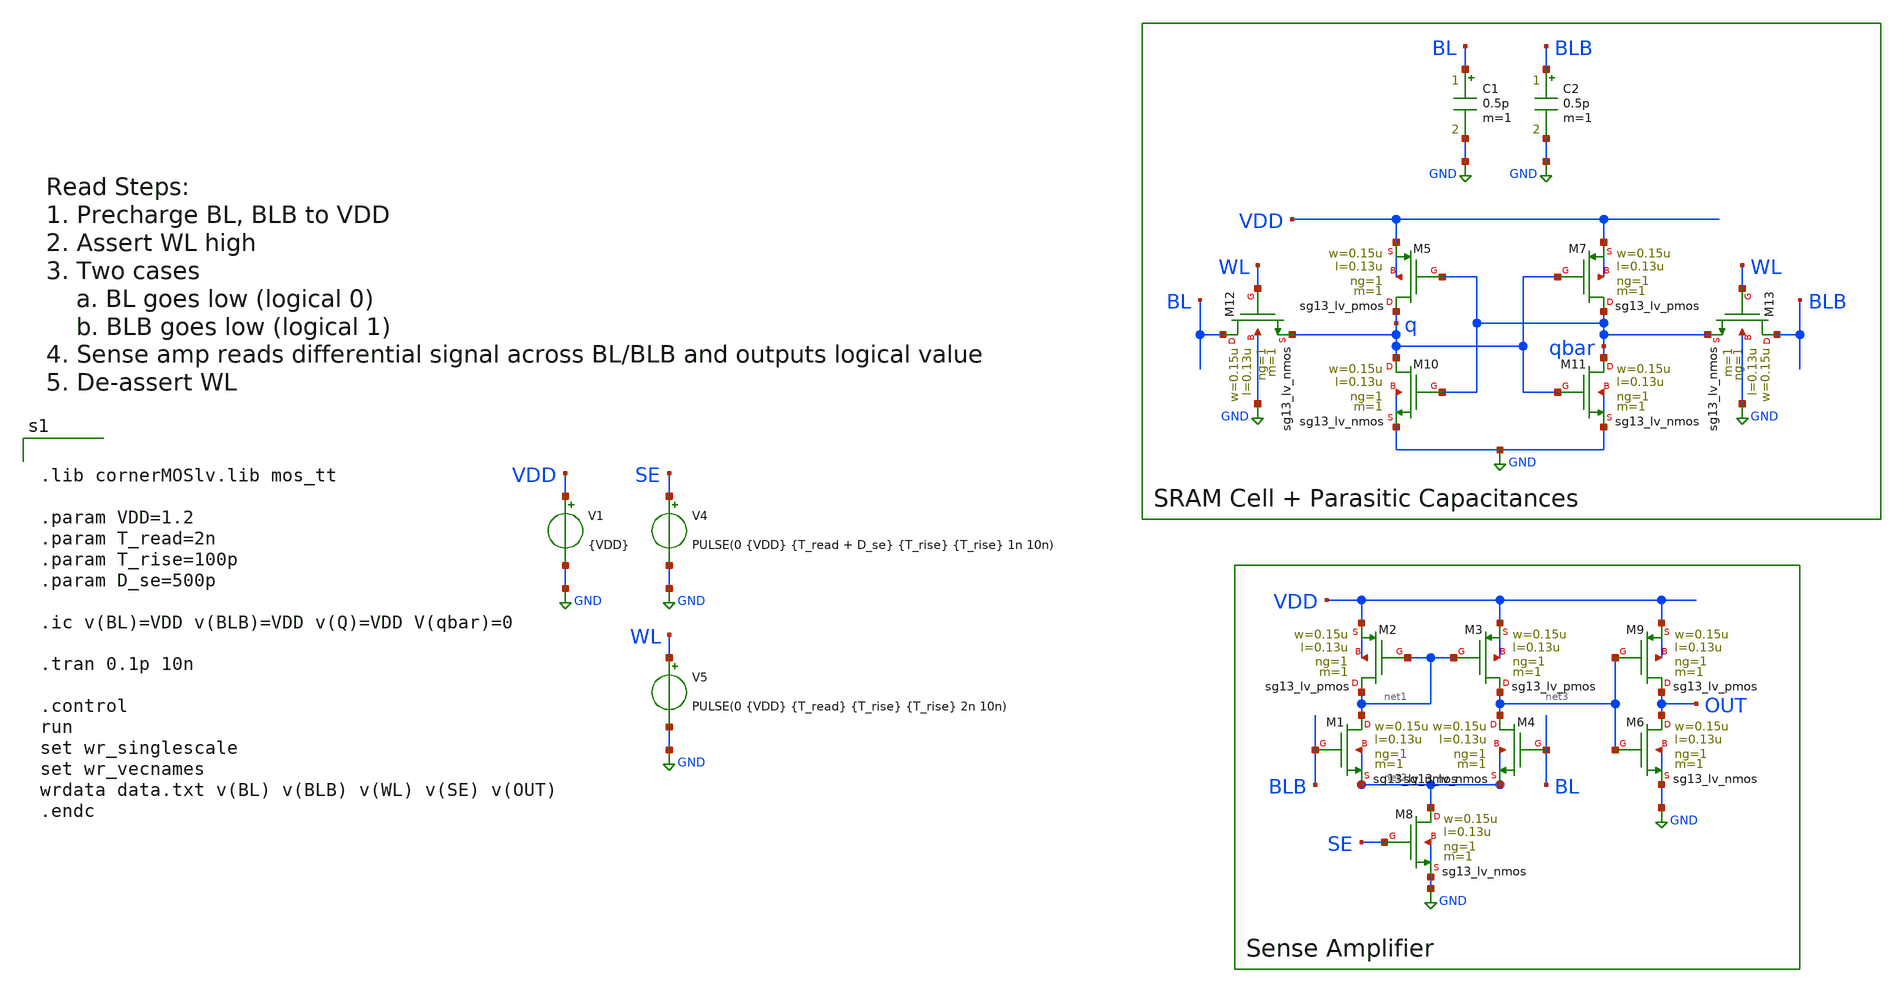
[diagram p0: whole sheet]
** sch_path: xschem/sram-sense-amp.sch
**.subckt sram-sense-amp
V1 VDD GND {VDD}
V4 SE GND PULSE(0 {VDD} {T_read + D_se} {T_rise} {T_rise} 1n 10n)
XM8 net2 SE GND GND sg13_lv_nmos w=0.15u l=0.13u ng=1 m=1 mm_ok=1
XM9 OUT net3 VDD VDD sg13_lv_pmos w=0.15u l=0.13u ng=1 m=1 mm_ok=1
XM1 net1 BLB net2 net2 sg13_lv_nmos w=0.15u l=0.13u ng=1 m=1 mm_ok=1
XM3 net3 net1 VDD VDD sg13_lv_pmos w=0.15u l=0.13u ng=1 m=1 mm_ok=1
XM2 net1 net1 VDD VDD sg13_lv_pmos w=0.15u l=0.13u ng=1 m=1 mm_ok=1
XM6 OUT net3 GND GND sg13_lv_nmos w=0.15u l=0.13u ng=1 m=1 mm_ok=1
XM4 net3 BL net2 net2 sg13_lv_nmos w=0.15u l=0.13u ng=1 m=1 mm_ok=1
XM5 q qbar VDD VDD sg13_lv_pmos w=0.15u l=0.13u ng=1 m=1 mm_ok=1
XM7 qbar q VDD VDD sg13_lv_pmos w=0.15u l=0.13u ng=1 m=1 mm_ok=1
XM10 q qbar GND GND sg13_lv_nmos w=0.15u l=0.13u ng=1 m=1 mm_ok=1
XM11 qbar q GND GND sg13_lv_nmos w=0.15u l=0.13u ng=1 m=1 mm_ok=1
XM12 BL WL q GND sg13_lv_nmos w=0.15u l=0.13u ng=1 m=1 mm_ok=1
XM13 BLB WL qbar GND sg13_lv_nmos w=0.15u l=0.13u ng=1 m=1 mm_ok=1
C1 BL GND 0.5p m=1
C2 BLB GND 0.5p m=1
V5 WL GND PULSE(0 {VDD} {T_read} {T_rise} {T_rise} 2n 10n)
**** begin user architecture code


.lib cornerMOSlv.lib mos_tt

.param VDD=1.2
.param T_read=2n
.param T_rise=100p
.param D_se=500p

.ic v(BL)=VDD v(BLB)=VDD v(Q)=VDD V(qbar)=0

.tran 0.1p 10n

.control
run
set wr_singlescale
set wr_vecnames
wrdata data.txt v(BL) v(BLB) v(WL) v(SE) v(OUT)
.endc


**** end user architecture code
**.ends
.GLOBAL GND
.end
